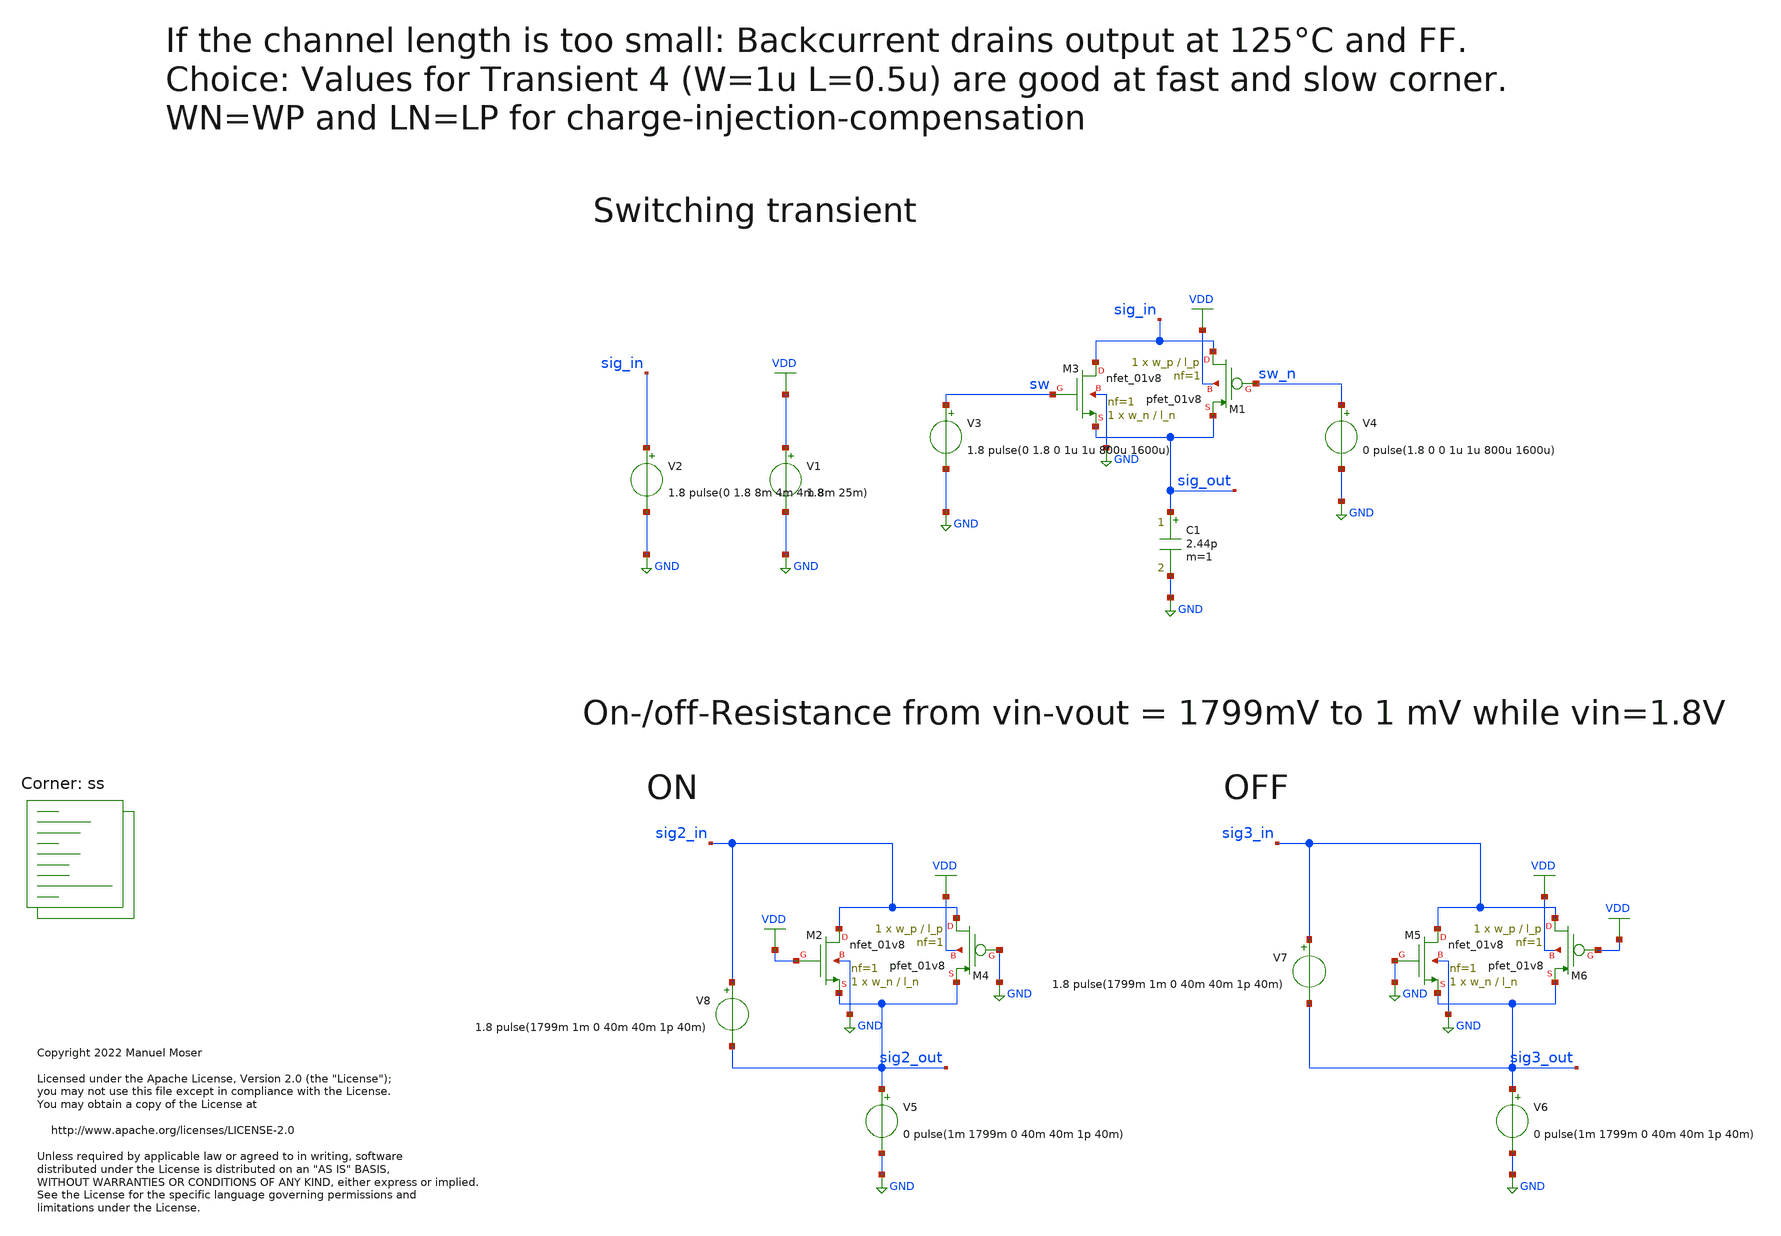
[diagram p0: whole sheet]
** sch_path: xschem/adc_vcm_switch_tb_resistance.sch
* Copyright 2022 Manuel Moser
* Licensed under the Apache License, Version 2.0 (the "License");
**.subckt adc_vcm_switch_tb_resistance
V1 VDD GND 1.8
V2 sig_in GND 1.8 pulse(0 1.8 8m 4m 4m 8m 25m)
V3 sw GND 1.8 pulse(0 1.8 0 1u 1u 800u 1600u)
V4 sw_n GND 0 pulse(1.8 0 0 1u 1u 800u 1600u)
C1 sig_out GND 2.44p m=1
V5 sig2_out GND 0 pulse(1m 1799m 0 40m 40m 1p 40m)
V6 sig3_out GND 0 pulse(1m 1799m 0 40m 40m 1p 40m)
V7 sig3_in sig3_out 1.8 pulse(1799m 1m 0 40m 40m 1p 40m)
V8 sig2_in sig2_out 1.8 pulse(1799m 1m 0 40m 40m 1p 40m)
XM1 sig_in sw_n sig_out VDD sky130_fd_pr__pfet_01v8 L=l_p W=w_p nf=1 ad='int((nf+1)/2) * W/nf * 0.29'
+ as='int((nf+2)/2) * W/nf * 0.29' pd='2*int((nf+1)/2) * (W/nf + 0.29)' ps='2*int((nf+2)/2) * (W/nf + 0.29)'
+ nrd='0.29 / W' nrs='0.29 / W' sa=0 sb=0 sd=0 mult=1 m=1
XM3 sig_in sw sig_out GND sky130_fd_pr__nfet_01v8 L=l_n W=w_n nf=1 ad='int((nf+1)/2) * W/nf * 0.29' as='int((nf+2)/2) * W/nf * 0.29'
+ pd='2*int((nf+1)/2) * (W/nf + 0.29)' ps='2*int((nf+2)/2) * (W/nf + 0.29)' nrd='0.29 / W' nrs='0.29 / W'
+ sa=0 sb=0 sd=0 mult=1 m=1
XM2 sig2_in VDD sig2_out GND sky130_fd_pr__nfet_01v8 L=l_n W=w_n nf=1 ad='int((nf+1)/2) * W/nf * 0.29'
+ as='int((nf+2)/2) * W/nf * 0.29' pd='2*int((nf+1)/2) * (W/nf + 0.29)' ps='2*int((nf+2)/2) * (W/nf + 0.29)'
+ nrd='0.29 / W' nrs='0.29 / W' sa=0 sb=0 sd=0 mult=1 m=1
XM4 sig2_in GND sig2_out VDD sky130_fd_pr__pfet_01v8 L=l_p W=w_p nf=1 ad='int((nf+1)/2) * W/nf * 0.29'
+ as='int((nf+2)/2) * W/nf * 0.29' pd='2*int((nf+1)/2) * (W/nf + 0.29)' ps='2*int((nf+2)/2) * (W/nf + 0.29)'
+ nrd='0.29 / W' nrs='0.29 / W' sa=0 sb=0 sd=0 mult=1 m=1
XM5 sig3_in GND sig3_out GND sky130_fd_pr__nfet_01v8 L=l_n W=w_n nf=1 ad='int((nf+1)/2) * W/nf * 0.29'
+ as='int((nf+2)/2) * W/nf * 0.29' pd='2*int((nf+1)/2) * (W/nf + 0.29)' ps='2*int((nf+2)/2) * (W/nf + 0.29)'
+ nrd='0.29 / W' nrs='0.29 / W' sa=0 sb=0 sd=0 mult=1 m=1
XM6 sig3_in VDD sig3_out VDD sky130_fd_pr__pfet_01v8 L=l_p W=w_p nf=1 ad='int((nf+1)/2) * W/nf * 0.29'
+ as='int((nf+2)/2) * W/nf * 0.29' pd='2*int((nf+1)/2) * (W/nf + 0.29)' ps='2*int((nf+2)/2) * (W/nf + 0.29)'
+ nrd='0.29 / W' nrs='0.29 / W' sa=0 sb=0 sd=0 mult=1 m=1
**** begin user architecture code
.lib $::SKYWATER_MODELS/sky130.lib.spice ss


.save all
.temp = -25
*.options method=gear
.OPTIONS savecurrents
.OPTIONS RELTOL=.1 TRTOL=1 ABSTOL=1e-20 CHGTOL=1.0e-20 DEFAD=1.0e-18
.save @m.x1.xm1.msky130_fd_pr__pfet_01v8[gm]
.save @m.x1.xm1.msky130_fd_pr__pfet_01v8[CGS]
.save @m.x1.xm1.msky130_fd_pr__pfet_01v8[Vth]
.save @m.x1.xm2.msky130_fd_pr__nfet_01v8_lvt[gm]
.save @m.x1.xm2.msky130_fd_pr__nfet_01v8_lvt[CGS]
.save @m.x1.xm2.msky130_fd_pr__nfet_01v8_lvt[Vth]


.param w_p=1
.param l_p = 1
.param w_n=1
.param l_n=1

.control
alterparam w_p=0.42
alterparam l_p=0.15
alterparam w_n=0.42
alterparam l_n=0.15
reset
tran 5u 40m 0 10u
write tran-sweep.out (-(v(sig2_in)-v(sig2_out))/I(v8)) (-(v(sig3_in)-v(sig3_out))/I(v7)) I(v7) I(v8)
set appendwrite


alterparam w_p=0.42
alterparam l_p=0.2
alterparam w_n=0.42
alterparam l_n=0.2
reset
tran 5u 40m 0 10u
write tran-sweep.out (-(v(sig2_in)-v(sig2_out))/I(v8)) (-(v(sig3_in)-v(sig3_out))/I(v7)) I(v7) I(v8)
set appendwrite


alterparam w_p=0.42
alterparam l_p=0.5
alterparam w_n=0.42
alterparam l_n=0.5
reset
tran 5u 40m 0 10u
write tran-sweep.out (-(v(sig2_in)-v(sig2_out))/I(v8)) (-(v(sig3_in)-v(sig3_out))/I(v7)) I(v7) I(v8)
set appendwrite

alterparam w_p=1
alterparam l_p=0.5
alterparam w_n=1
alterparam l_n=0.5
reset
tran 5u 40m 0 10u
write tran-sweep.out (-(v(sig2_in)-v(sig2_out))/I(v8)) (-(v(sig3_in)-v(sig3_out))/I(v7)) I(v7) I(v8)
set appendwrite


plot tran1.v(sig_in) tran1.v(sig_out) tran2.v(sig_out) tran3.v(sig_out) tran4.v(sig_out)
plot (-(tran1.v(sig2_in)-tran1.v(sig2_out))/tran1.I(v8))
+ (-(tran2.v(sig2_in)-tran2.v(sig2_out))/tran2.I(v8)) (-(tran3.v(sig2_in)-tran3.v(sig2_out))/tran3.I(v8))
+ (-(tran4.v(sig2_in)-tran4.v(sig2_out))/tran4.I(v8))
plot (-(tran1.v(sig3_in)-tran1.v(sig3_out))/tran1.I(v7))
+ (-(tran2.v(sig3_in)-tran2.v(sig3_out))/tran2.I(v7)) (-(tran3.v(sig3_in)-tran3.v(sig3_out))/tran3.I(v7))
+ (-(tran4.v(sig3_in)-tran4.v(sig3_out))/tran4.I(v7))
.endc


**** end user architecture code
**.ends
.GLOBAL GND
.GLOBAL VDD
.end
